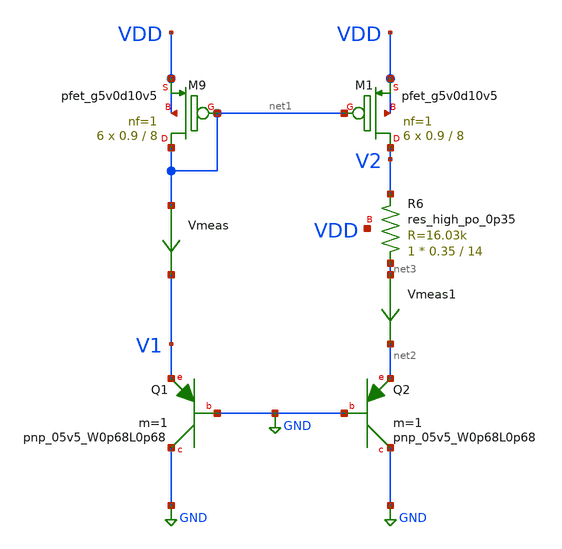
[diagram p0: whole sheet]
** sch_path: my_projects/V_REF/basic_PTAT/V_ref1.sch
**.subckt V_ref1
XQ1 GND GND V1 sky130_fd_pr__pnp_05v5_W0p68L0p68 m=1
XM9 net1 net1 VDD VDD sky130_fd_pr__pfet_g5v0d10v5 L=8 W=0.9 nf=1 ad='int((1 + 1)/2) * 0.9 / 1 * 0.29'
+ as='int((1 + 2)/2) * 0.9 / 1 * 0.29' pd='2*int((1 + 1)/2) * (0.9 / 1 + 0.29)' ps='2*int((1 + 2)/2) * (0.9 / 1 + 0.29)'
+ nrd='0.29 / 0.9 ' nrs='0.29 / 0.9 ' sa=0 sb=0 sd=0 mult=6 m=6
Vmeas net1 V1 0
.save i(vmeas)
XM1 V2 net1 VDD VDD sky130_fd_pr__pfet_g5v0d10v5 L=8 W=0.9 nf=1 ad='int((1 + 1)/2) * 0.9 / 1 * 0.29'
+ as='int((1 + 2)/2) * 0.9 / 1 * 0.29' pd='2*int((1 + 1)/2) * (0.9 / 1 + 0.29)' ps='2*int((1 + 2)/2) * (0.9 / 1 + 0.29)'
+ nrd='0.29 / 0.9 ' nrs='0.29 / 0.9 ' sa=0 sb=0 sd=0 mult=6 m=6
XQ2 GND GND net2 sky130_fd_pr__pnp_05v5_W0p68L0p68 m=1
Vmeas1 net3 net2 0
.save i(vmeas1)
XR6 net3 V2 VDD sky130_fd_pr__res_high_po_0p35 L=14 mult=1 m=1
**.ends
.GLOBAL GND
.end
